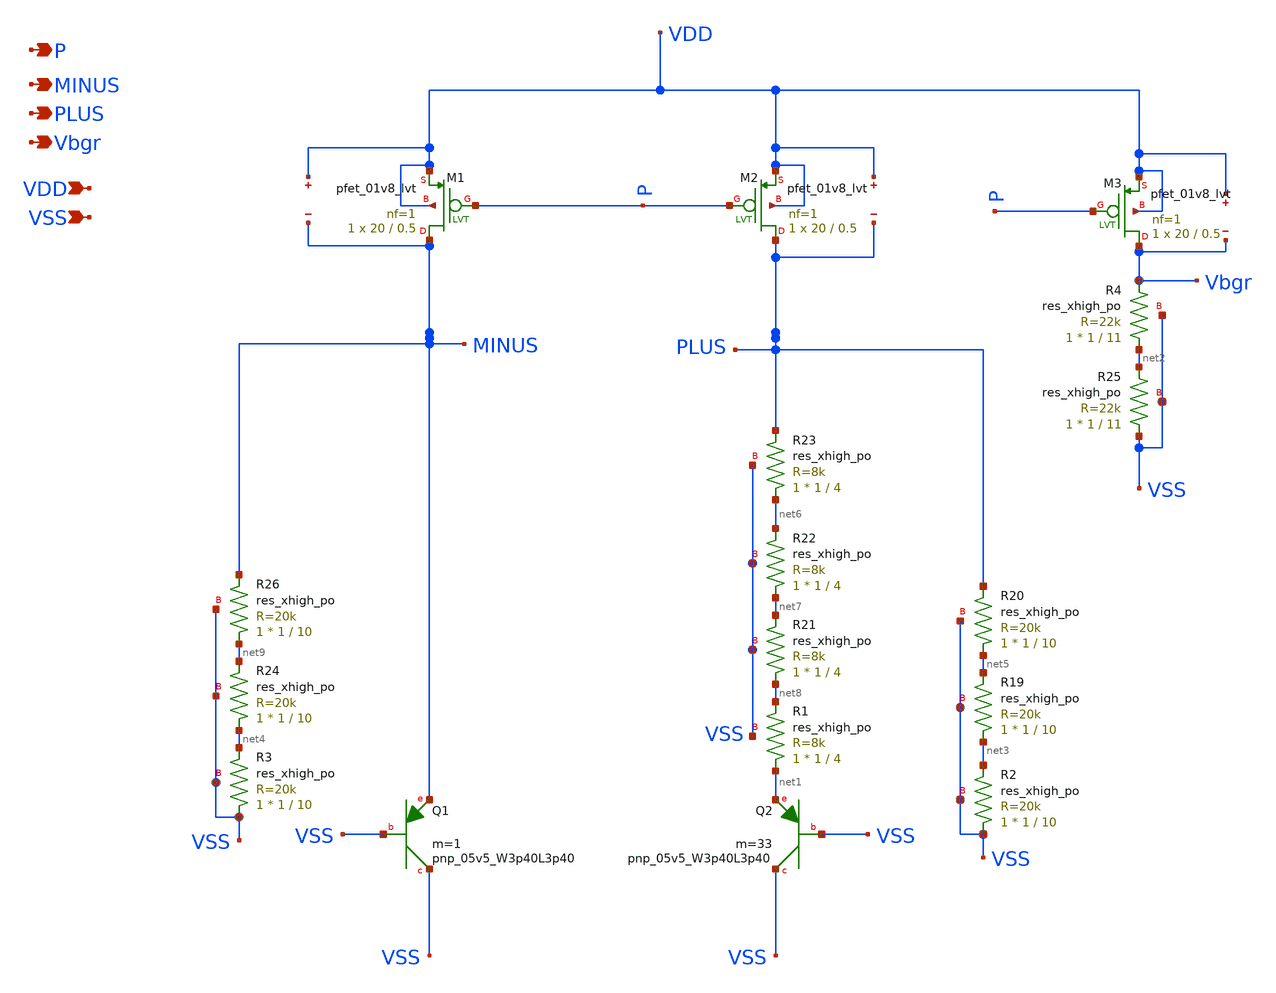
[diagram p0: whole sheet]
** sch_path: xschem/core.sch
**.subckt core MINUS PLUS Vbgr VDD VSS P
*.opin MINUS
*.opin PLUS
*.opin Vbgr
*.ipin VDD
*.ipin VSS
*.opin P
XQ1 VSS VSS MINUS sky130_fd_pr__pnp_05v5_W3p40L3p40 m=1
XQ2 VSS VSS net1 sky130_fd_pr__pnp_05v5_W3p40L3p40 m=33
XM1 MINUS P VDD VDD sky130_fd_pr__pfet_01v8_lvt L=0.5 W=20 nf=1 ad='int((nf+1)/2) * W/nf * 0.29' as='int((nf+2)/2) * W/nf * 0.29'
+ pd='2*int((nf+1)/2) * (W/nf + 0.29)' ps='2*int((nf+2)/2) * (W/nf + 0.29)' nrd='0.29 / W' nrs='0.29 / W'
+ sa=0 sb=0 sd=0 mult=1 m=1
XM2 PLUS P VDD VDD sky130_fd_pr__pfet_01v8_lvt L=0.5 W=20 nf=1 ad='int((nf+1)/2) * W/nf * 0.29' as='int((nf+2)/2) * W/nf * 0.29'
+ pd='2*int((nf+1)/2) * (W/nf + 0.29)' ps='2*int((nf+2)/2) * (W/nf + 0.29)' nrd='0.29 / W' nrs='0.29 / W'
+ sa=0 sb=0 sd=0 mult=1 m=1
XM3 Vbgr P VDD VDD sky130_fd_pr__pfet_01v8_lvt L=0.5 W=20 nf=1 ad='int((nf+1)/2) * W/nf * 0.29' as='int((nf+2)/2) * W/nf * 0.29'
+ pd='2*int((nf+1)/2) * (W/nf + 0.29)' ps='2*int((nf+2)/2) * (W/nf + 0.29)' nrd='0.29 / W' nrs='0.29 / W'
+ sa=0 sb=0 sd=0 mult=1 m=1
.save v(vdd)
.save v(minus)
.save v(vdd)
.save v(plus)
.save v(vdd)
.save v(vbgr)
XR2 VSS net3 VSS sky130_fd_pr__res_xhigh_po W=1 L=10 mult=1 m=1
XR3 VSS net4 VSS sky130_fd_pr__res_xhigh_po W=1 L=10 mult=1 m=1
XR4 net2 Vbgr VSS sky130_fd_pr__res_xhigh_po W=1 L=11 mult=1 m=1
XR25 VSS net2 VSS sky130_fd_pr__res_xhigh_po W=1 L=11 mult=1 m=1
XR1 net1 net8 VSS sky130_fd_pr__res_xhigh_po W=1 L=4 mult=1 m=1
XR19 net3 net5 VSS sky130_fd_pr__res_xhigh_po W=1 L=10 mult=1 m=1
XR20 net5 PLUS VSS sky130_fd_pr__res_xhigh_po W=1 L=10 mult=1 m=1
XR21 net8 net7 VSS sky130_fd_pr__res_xhigh_po W=1 L=4 mult=1 m=1
XR22 net7 net6 VSS sky130_fd_pr__res_xhigh_po W=1 L=4 mult=1 m=1
XR23 net6 PLUS VSS sky130_fd_pr__res_xhigh_po W=1 L=4 mult=1 m=1
XR24 net4 net9 VSS sky130_fd_pr__res_xhigh_po W=1 L=10 mult=1 m=1
XR26 net9 MINUS VSS sky130_fd_pr__res_xhigh_po W=1 L=10 mult=1 m=1
**.ends
.end
